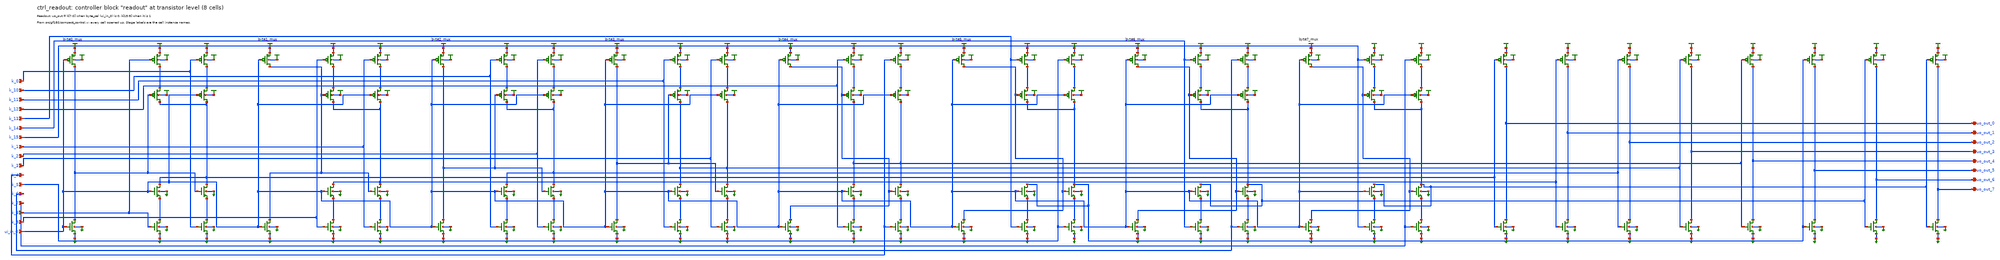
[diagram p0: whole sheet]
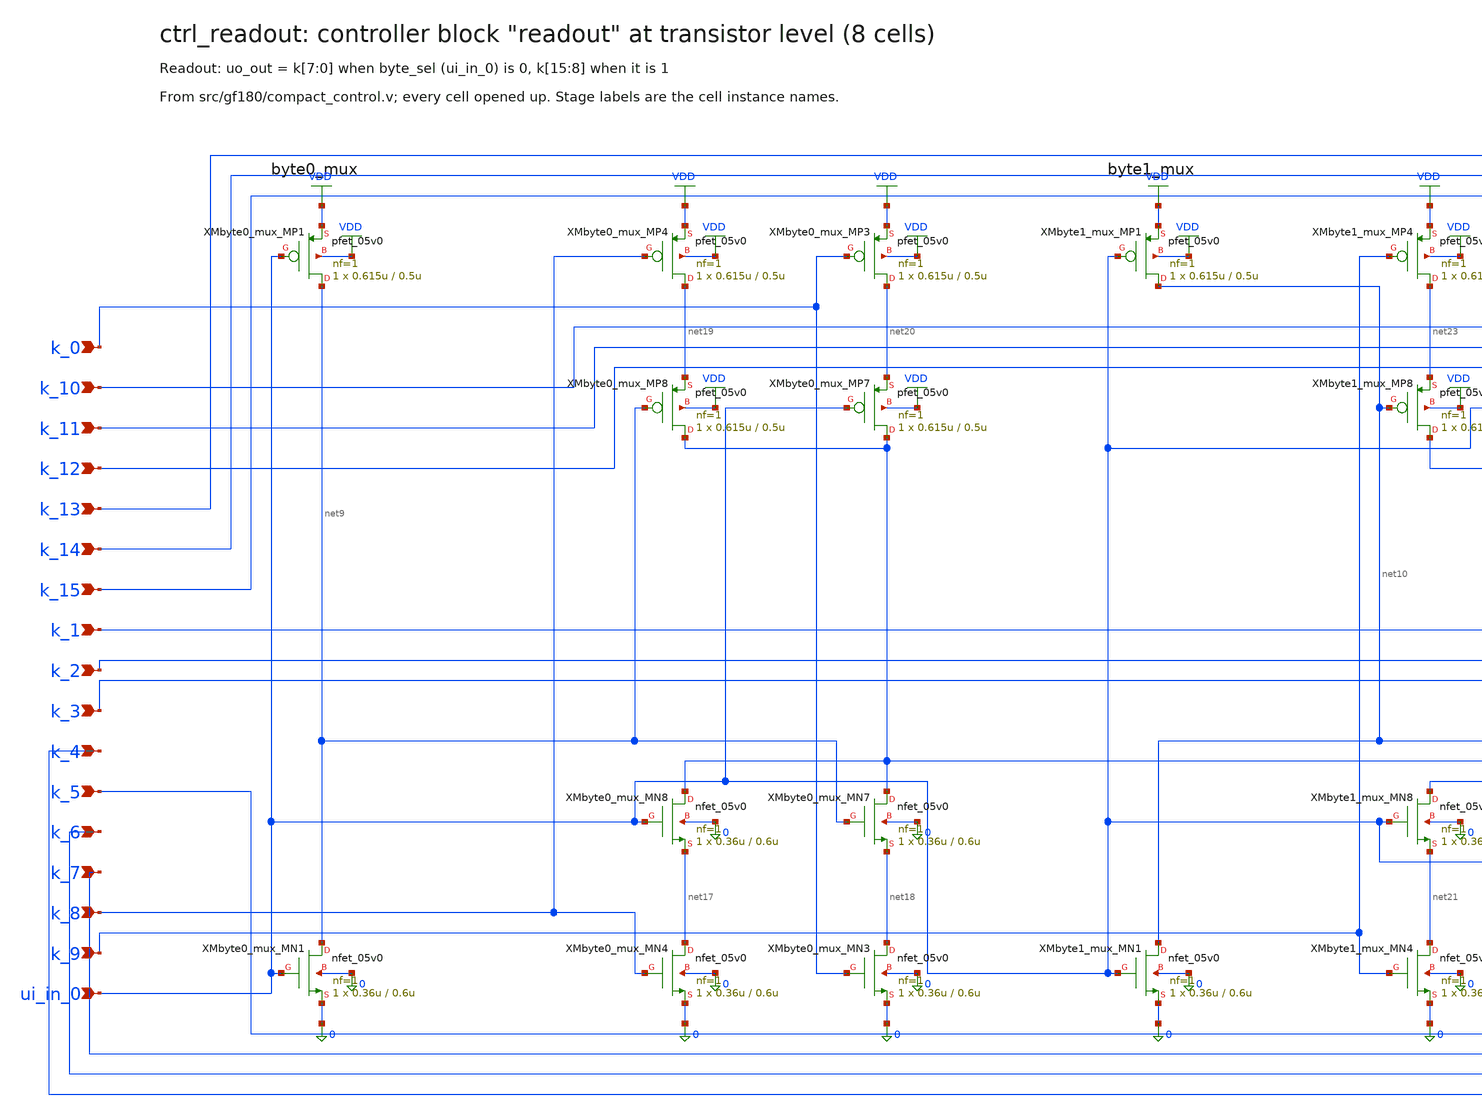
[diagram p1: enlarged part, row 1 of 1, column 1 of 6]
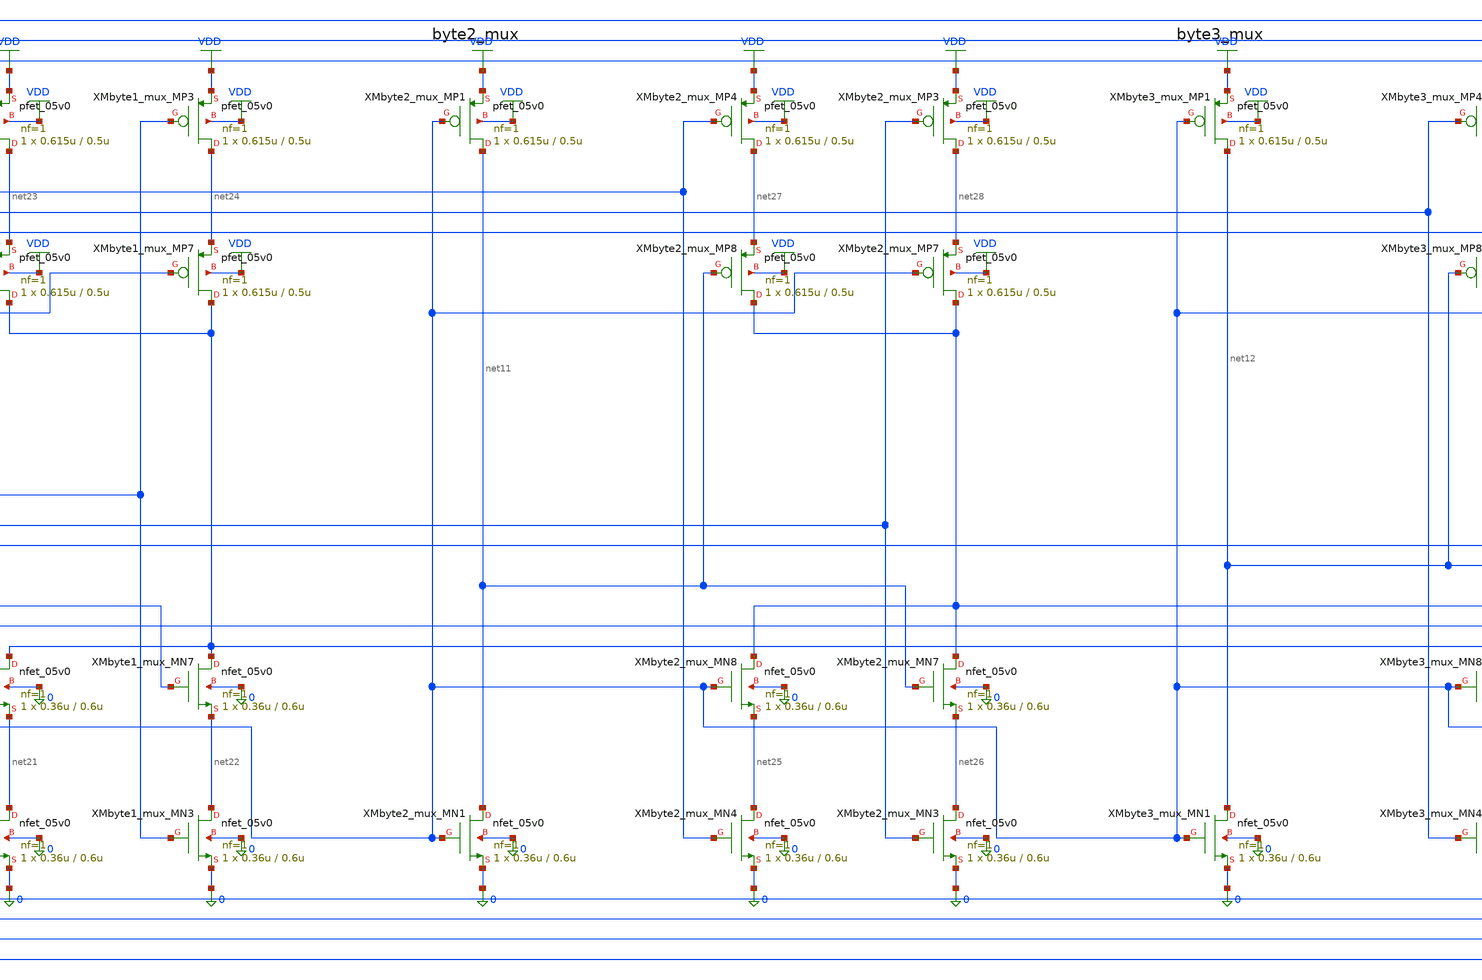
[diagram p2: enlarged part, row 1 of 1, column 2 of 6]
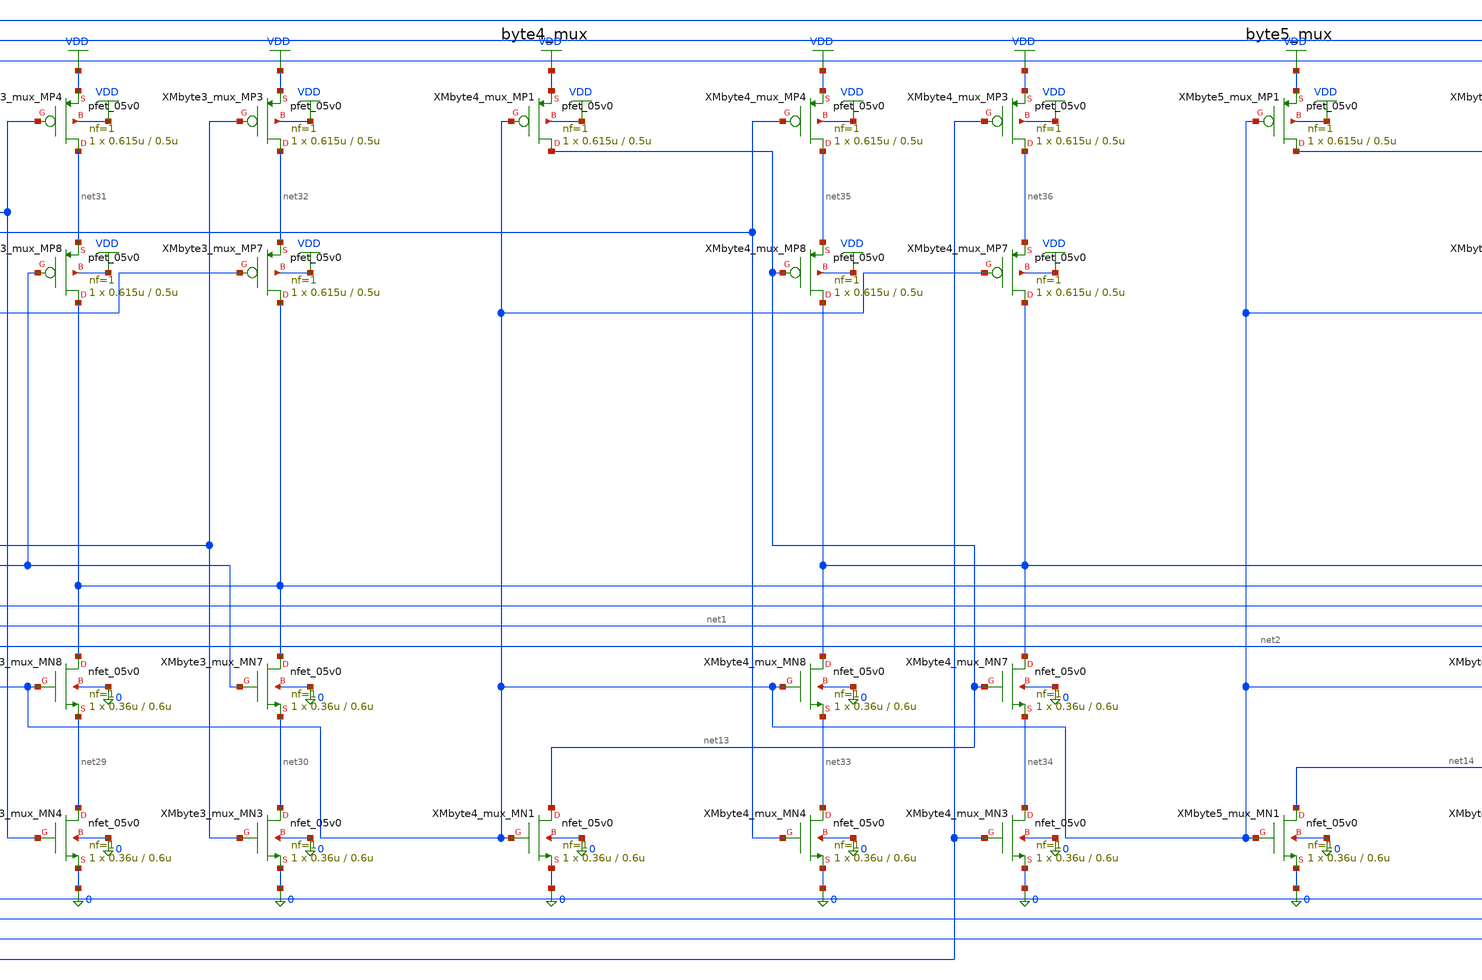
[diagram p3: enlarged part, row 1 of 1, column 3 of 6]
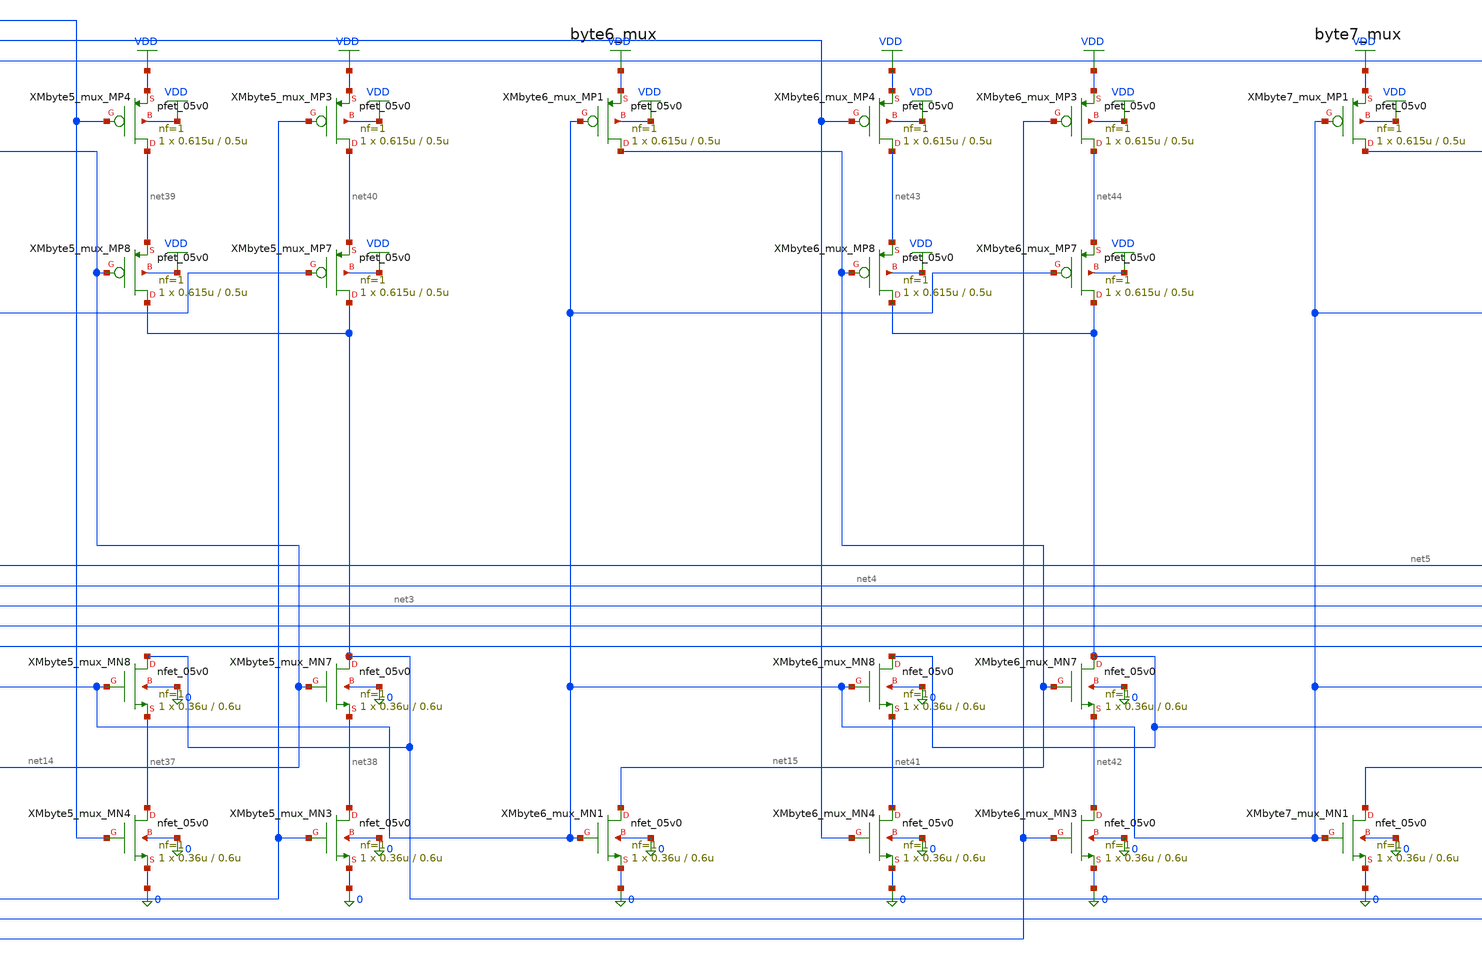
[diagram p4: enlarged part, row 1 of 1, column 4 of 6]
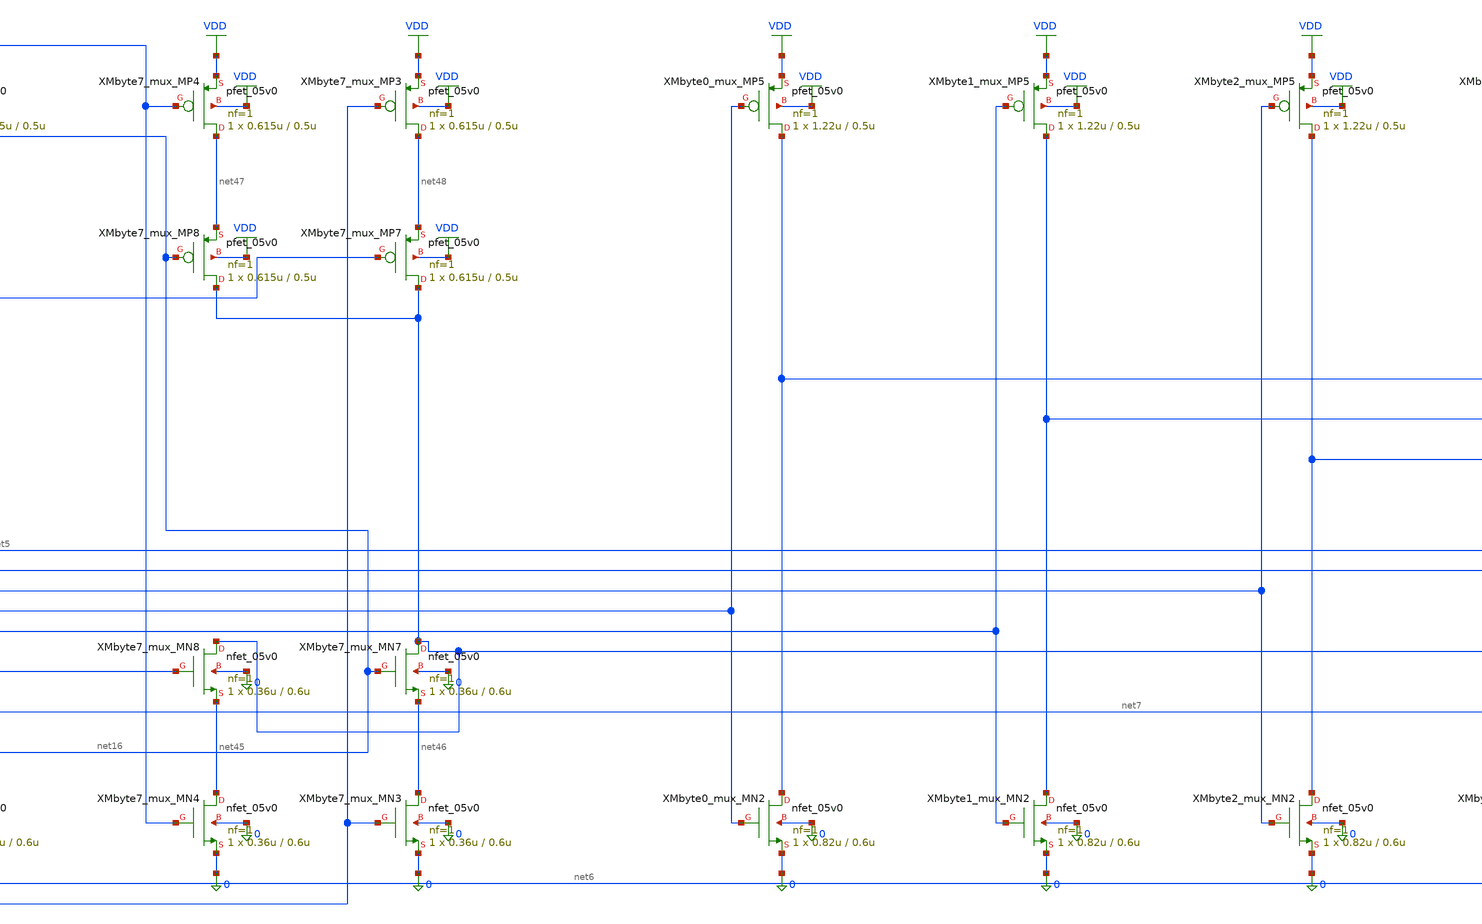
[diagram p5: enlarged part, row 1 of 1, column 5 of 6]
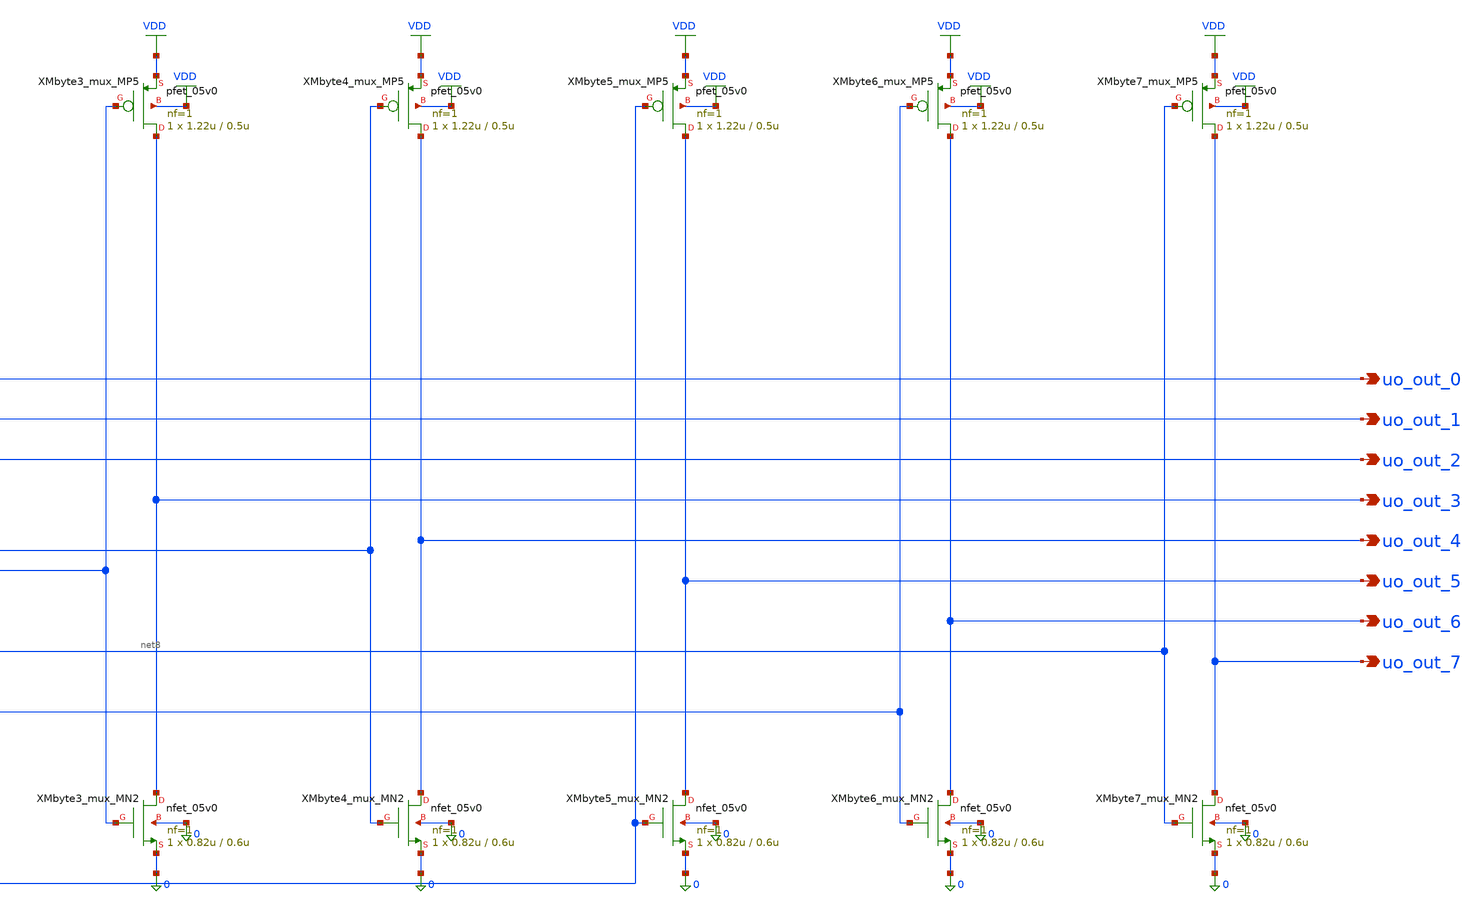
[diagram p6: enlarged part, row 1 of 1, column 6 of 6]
** sch_path: xschem/flat/ctrl_readout.sch
**.subckt ctrl_readout k_0 k_10 k_11 k_12 k_13 k_14 k_15 k_1 k_2 k_3 k_4 k_5 k_6 k_7 k_8 k_9 ui_in_0
*+ uo_out_0 uo_out_1 uo_out_2 uo_out_3 uo_out_4 uo_out_5 uo_out_6 uo_out_7
*.ipin k_0
*.ipin k_10
*.ipin k_11
*.ipin k_12
*.ipin k_13
*.ipin k_14
*.ipin k_15
*.ipin k_1
*.ipin k_2
*.ipin k_3
*.ipin k_4
*.ipin k_5
*.ipin k_6
*.ipin k_7
*.ipin k_8
*.ipin k_9
*.ipin ui_in_0
*.opin uo_out_0
*.opin uo_out_1
*.opin uo_out_2
*.opin uo_out_3
*.opin uo_out_4
*.opin uo_out_5
*.opin uo_out_6
*.opin uo_out_7
XMbyte0_mux_MN2 uo_out_0 net1 0 0 nfet_05v0 L=0.6u W=0.82u nf=1 ad=4.1e-13 as=4.1e-13 pd=2.64e-06
+ ps=2.64e-06 nrd=0 nrs=0 sa=0 sb=0 sd=0 m=1
XMbyte0_mux_MN4 net17 k_8 0 0 nfet_05v0 L=0.6u W=0.36u nf=1 ad=1.8e-13 as=1.8e-13 pd=1.72e-06
+ ps=1.72e-06 nrd=0 nrs=0 sa=0 sb=0 sd=0 m=1
XMbyte0_mux_MN8 net1 ui_in_0 net17 0 nfet_05v0 L=0.6u W=0.36u nf=1 ad=1.8e-13 as=1.8e-13 pd=1.72e-06
+ ps=1.72e-06 nrd=0 nrs=0 sa=0 sb=0 sd=0 m=1
XMbyte0_mux_MN7 net1 net9 net18 0 nfet_05v0 L=0.6u W=0.36u nf=1 ad=1.8e-13 as=1.8e-13 pd=1.72e-06
+ ps=1.72e-06 nrd=0 nrs=0 sa=0 sb=0 sd=0 m=1
XMbyte0_mux_MN3 net18 k_0 0 0 nfet_05v0 L=0.6u W=0.36u nf=1 ad=1.8e-13 as=1.8e-13 pd=1.72e-06
+ ps=1.72e-06 nrd=0 nrs=0 sa=0 sb=0 sd=0 m=1
XMbyte0_mux_MN1 net9 ui_in_0 0 0 nfet_05v0 L=0.6u W=0.36u nf=1 ad=1.8e-13 as=1.8e-13 pd=1.72e-06
+ ps=1.72e-06 nrd=0 nrs=0 sa=0 sb=0 sd=0 m=1
XMbyte0_mux_MP5 uo_out_0 net1 VDD VDD pfet_05v0 L=0.5u W=1.22u nf=1 ad=6.1e-13 as=6.1e-13
+ pd=3.44e-06 ps=3.44e-06 nrd=0 nrs=0 sa=0 sb=0 sd=0 m=1
XMbyte0_mux_MP4 net19 k_8 VDD VDD pfet_05v0 L=0.5u W=0.615u nf=1 ad=3.075e-13 as=3.075e-13
+ pd=2.23e-06 ps=2.23e-06 nrd=0 nrs=0 sa=0 sb=0 sd=0 m=1
XMbyte0_mux_MP8 net1 net9 net19 VDD pfet_05v0 L=0.5u W=0.615u nf=1 ad=3.075e-13 as=3.075e-13
+ pd=2.23e-06 ps=2.23e-06 nrd=0 nrs=0 sa=0 sb=0 sd=0 m=1
XMbyte0_mux_MP7 net1 ui_in_0 net20 VDD pfet_05v0 L=0.5u W=0.615u nf=1 ad=3.075e-13 as=3.075e-13
+ pd=2.23e-06 ps=2.23e-06 nrd=0 nrs=0 sa=0 sb=0 sd=0 m=1
XMbyte0_mux_MP3 net20 k_0 VDD VDD pfet_05v0 L=0.5u W=0.615u nf=1 ad=3.075e-13 as=3.075e-13
+ pd=2.23e-06 ps=2.23e-06 nrd=0 nrs=0 sa=0 sb=0 sd=0 m=1
XMbyte0_mux_MP1 net9 ui_in_0 VDD VDD pfet_05v0 L=0.5u W=0.615u nf=1 ad=3.075e-13 as=3.075e-13
+ pd=2.23e-06 ps=2.23e-06 nrd=0 nrs=0 sa=0 sb=0 sd=0 m=1
XMbyte1_mux_MN2 uo_out_1 net2 0 0 nfet_05v0 L=0.6u W=0.82u nf=1 ad=4.1e-13 as=4.1e-13 pd=2.64e-06
+ ps=2.64e-06 nrd=0 nrs=0 sa=0 sb=0 sd=0 m=1
XMbyte1_mux_MN4 net21 k_9 0 0 nfet_05v0 L=0.6u W=0.36u nf=1 ad=1.8e-13 as=1.8e-13 pd=1.72e-06
+ ps=1.72e-06 nrd=0 nrs=0 sa=0 sb=0 sd=0 m=1
XMbyte1_mux_MN8 net2 ui_in_0 net21 0 nfet_05v0 L=0.6u W=0.36u nf=1 ad=1.8e-13 as=1.8e-13 pd=1.72e-06
+ ps=1.72e-06 nrd=0 nrs=0 sa=0 sb=0 sd=0 m=1
XMbyte1_mux_MN7 net2 net10 net22 0 nfet_05v0 L=0.6u W=0.36u nf=1 ad=1.8e-13 as=1.8e-13 pd=1.72e-06
+ ps=1.72e-06 nrd=0 nrs=0 sa=0 sb=0 sd=0 m=1
XMbyte1_mux_MN3 net22 k_1 0 0 nfet_05v0 L=0.6u W=0.36u nf=1 ad=1.8e-13 as=1.8e-13 pd=1.72e-06
+ ps=1.72e-06 nrd=0 nrs=0 sa=0 sb=0 sd=0 m=1
XMbyte1_mux_MN1 net10 ui_in_0 0 0 nfet_05v0 L=0.6u W=0.36u nf=1 ad=1.8e-13 as=1.8e-13 pd=1.72e-06
+ ps=1.72e-06 nrd=0 nrs=0 sa=0 sb=0 sd=0 m=1
XMbyte1_mux_MP5 uo_out_1 net2 VDD VDD pfet_05v0 L=0.5u W=1.22u nf=1 ad=6.1e-13 as=6.1e-13
+ pd=3.44e-06 ps=3.44e-06 nrd=0 nrs=0 sa=0 sb=0 sd=0 m=1
XMbyte1_mux_MP4 net23 k_9 VDD VDD pfet_05v0 L=0.5u W=0.615u nf=1 ad=3.075e-13 as=3.075e-13
+ pd=2.23e-06 ps=2.23e-06 nrd=0 nrs=0 sa=0 sb=0 sd=0 m=1
XMbyte1_mux_MP8 net2 net10 net23 VDD pfet_05v0 L=0.5u W=0.615u nf=1 ad=3.075e-13 as=3.075e-13
+ pd=2.23e-06 ps=2.23e-06 nrd=0 nrs=0 sa=0 sb=0 sd=0 m=1
XMbyte1_mux_MP7 net2 ui_in_0 net24 VDD pfet_05v0 L=0.5u W=0.615u nf=1 ad=3.075e-13 as=3.075e-13
+ pd=2.23e-06 ps=2.23e-06 nrd=0 nrs=0 sa=0 sb=0 sd=0 m=1
XMbyte1_mux_MP3 net24 k_1 VDD VDD pfet_05v0 L=0.5u W=0.615u nf=1 ad=3.075e-13 as=3.075e-13
+ pd=2.23e-06 ps=2.23e-06 nrd=0 nrs=0 sa=0 sb=0 sd=0 m=1
XMbyte1_mux_MP1 net10 ui_in_0 VDD VDD pfet_05v0 L=0.5u W=0.615u nf=1 ad=3.075e-13 as=3.075e-13
+ pd=2.23e-06 ps=2.23e-06 nrd=0 nrs=0 sa=0 sb=0 sd=0 m=1
XMbyte2_mux_MN2 uo_out_2 net3 0 0 nfet_05v0 L=0.6u W=0.82u nf=1 ad=4.1e-13 as=4.1e-13 pd=2.64e-06
+ ps=2.64e-06 nrd=0 nrs=0 sa=0 sb=0 sd=0 m=1
XMbyte2_mux_MN4 net25 k_10 0 0 nfet_05v0 L=0.6u W=0.36u nf=1 ad=1.8e-13 as=1.8e-13 pd=1.72e-06
+ ps=1.72e-06 nrd=0 nrs=0 sa=0 sb=0 sd=0 m=1
XMbyte2_mux_MN8 net3 ui_in_0 net25 0 nfet_05v0 L=0.6u W=0.36u nf=1 ad=1.8e-13 as=1.8e-13 pd=1.72e-06
+ ps=1.72e-06 nrd=0 nrs=0 sa=0 sb=0 sd=0 m=1
XMbyte2_mux_MN7 net3 net11 net26 0 nfet_05v0 L=0.6u W=0.36u nf=1 ad=1.8e-13 as=1.8e-13 pd=1.72e-06
+ ps=1.72e-06 nrd=0 nrs=0 sa=0 sb=0 sd=0 m=1
XMbyte2_mux_MN3 net26 k_2 0 0 nfet_05v0 L=0.6u W=0.36u nf=1 ad=1.8e-13 as=1.8e-13 pd=1.72e-06
+ ps=1.72e-06 nrd=0 nrs=0 sa=0 sb=0 sd=0 m=1
XMbyte2_mux_MN1 net11 ui_in_0 0 0 nfet_05v0 L=0.6u W=0.36u nf=1 ad=1.8e-13 as=1.8e-13 pd=1.72e-06
+ ps=1.72e-06 nrd=0 nrs=0 sa=0 sb=0 sd=0 m=1
XMbyte2_mux_MP5 uo_out_2 net3 VDD VDD pfet_05v0 L=0.5u W=1.22u nf=1 ad=6.1e-13 as=6.1e-13
+ pd=3.44e-06 ps=3.44e-06 nrd=0 nrs=0 sa=0 sb=0 sd=0 m=1
XMbyte2_mux_MP4 net27 k_10 VDD VDD pfet_05v0 L=0.5u W=0.615u nf=1 ad=3.075e-13 as=3.075e-13
+ pd=2.23e-06 ps=2.23e-06 nrd=0 nrs=0 sa=0 sb=0 sd=0 m=1
XMbyte2_mux_MP8 net3 net11 net27 VDD pfet_05v0 L=0.5u W=0.615u nf=1 ad=3.075e-13 as=3.075e-13
+ pd=2.23e-06 ps=2.23e-06 nrd=0 nrs=0 sa=0 sb=0 sd=0 m=1
XMbyte2_mux_MP7 net3 ui_in_0 net28 VDD pfet_05v0 L=0.5u W=0.615u nf=1 ad=3.075e-13 as=3.075e-13
+ pd=2.23e-06 ps=2.23e-06 nrd=0 nrs=0 sa=0 sb=0 sd=0 m=1
XMbyte2_mux_MP3 net28 k_2 VDD VDD pfet_05v0 L=0.5u W=0.615u nf=1 ad=3.075e-13 as=3.075e-13
+ pd=2.23e-06 ps=2.23e-06 nrd=0 nrs=0 sa=0 sb=0 sd=0 m=1
XMbyte2_mux_MP1 net11 ui_in_0 VDD VDD pfet_05v0 L=0.5u W=0.615u nf=1 ad=3.075e-13 as=3.075e-13
+ pd=2.23e-06 ps=2.23e-06 nrd=0 nrs=0 sa=0 sb=0 sd=0 m=1
XMbyte3_mux_MN2 uo_out_3 net4 0 0 nfet_05v0 L=0.6u W=0.82u nf=1 ad=4.1e-13 as=4.1e-13 pd=2.64e-06
+ ps=2.64e-06 nrd=0 nrs=0 sa=0 sb=0 sd=0 m=1
XMbyte3_mux_MN4 net29 k_11 0 0 nfet_05v0 L=0.6u W=0.36u nf=1 ad=1.8e-13 as=1.8e-13 pd=1.72e-06
+ ps=1.72e-06 nrd=0 nrs=0 sa=0 sb=0 sd=0 m=1
XMbyte3_mux_MN8 net4 ui_in_0 net29 0 nfet_05v0 L=0.6u W=0.36u nf=1 ad=1.8e-13 as=1.8e-13 pd=1.72e-06
+ ps=1.72e-06 nrd=0 nrs=0 sa=0 sb=0 sd=0 m=1
XMbyte3_mux_MN7 net4 net12 net30 0 nfet_05v0 L=0.6u W=0.36u nf=1 ad=1.8e-13 as=1.8e-13 pd=1.72e-06
+ ps=1.72e-06 nrd=0 nrs=0 sa=0 sb=0 sd=0 m=1
XMbyte3_mux_MN3 net30 k_3 0 0 nfet_05v0 L=0.6u W=0.36u nf=1 ad=1.8e-13 as=1.8e-13 pd=1.72e-06
+ ps=1.72e-06 nrd=0 nrs=0 sa=0 sb=0 sd=0 m=1
XMbyte3_mux_MN1 net12 ui_in_0 0 0 nfet_05v0 L=0.6u W=0.36u nf=1 ad=1.8e-13 as=1.8e-13 pd=1.72e-06
+ ps=1.72e-06 nrd=0 nrs=0 sa=0 sb=0 sd=0 m=1
XMbyte3_mux_MP5 uo_out_3 net4 VDD VDD pfet_05v0 L=0.5u W=1.22u nf=1 ad=6.1e-13 as=6.1e-13
+ pd=3.44e-06 ps=3.44e-06 nrd=0 nrs=0 sa=0 sb=0 sd=0 m=1
XMbyte3_mux_MP4 net31 k_11 VDD VDD pfet_05v0 L=0.5u W=0.615u nf=1 ad=3.075e-13 as=3.075e-13
+ pd=2.23e-06 ps=2.23e-06 nrd=0 nrs=0 sa=0 sb=0 sd=0 m=1
XMbyte3_mux_MP8 net4 net12 net31 VDD pfet_05v0 L=0.5u W=0.615u nf=1 ad=3.075e-13 as=3.075e-13
+ pd=2.23e-06 ps=2.23e-06 nrd=0 nrs=0 sa=0 sb=0 sd=0 m=1
XMbyte3_mux_MP7 net4 ui_in_0 net32 VDD pfet_05v0 L=0.5u W=0.615u nf=1 ad=3.075e-13 as=3.075e-13
+ pd=2.23e-06 ps=2.23e-06 nrd=0 nrs=0 sa=0 sb=0 sd=0 m=1
XMbyte3_mux_MP3 net32 k_3 VDD VDD pfet_05v0 L=0.5u W=0.615u nf=1 ad=3.075e-13 as=3.075e-13
+ pd=2.23e-06 ps=2.23e-06 nrd=0 nrs=0 sa=0 sb=0 sd=0 m=1
XMbyte3_mux_MP1 net12 ui_in_0 VDD VDD pfet_05v0 L=0.5u W=0.615u nf=1 ad=3.075e-13 as=3.075e-13
+ pd=2.23e-06 ps=2.23e-06 nrd=0 nrs=0 sa=0 sb=0 sd=0 m=1
XMbyte4_mux_MN2 uo_out_4 net5 0 0 nfet_05v0 L=0.6u W=0.82u nf=1 ad=4.1e-13 as=4.1e-13 pd=2.64e-06
+ ps=2.64e-06 nrd=0 nrs=0 sa=0 sb=0 sd=0 m=1
XMbyte4_mux_MN4 net33 k_12 0 0 nfet_05v0 L=0.6u W=0.36u nf=1 ad=1.8e-13 as=1.8e-13 pd=1.72e-06
+ ps=1.72e-06 nrd=0 nrs=0 sa=0 sb=0 sd=0 m=1
XMbyte4_mux_MN8 net5 ui_in_0 net33 0 nfet_05v0 L=0.6u W=0.36u nf=1 ad=1.8e-13 as=1.8e-13 pd=1.72e-06
+ ps=1.72e-06 nrd=0 nrs=0 sa=0 sb=0 sd=0 m=1
XMbyte4_mux_MN7 net5 net13 net34 0 nfet_05v0 L=0.6u W=0.36u nf=1 ad=1.8e-13 as=1.8e-13 pd=1.72e-06
+ ps=1.72e-06 nrd=0 nrs=0 sa=0 sb=0 sd=0 m=1
XMbyte4_mux_MN3 net34 k_4 0 0 nfet_05v0 L=0.6u W=0.36u nf=1 ad=1.8e-13 as=1.8e-13 pd=1.72e-06
+ ps=1.72e-06 nrd=0 nrs=0 sa=0 sb=0 sd=0 m=1
XMbyte4_mux_MN1 net13 ui_in_0 0 0 nfet_05v0 L=0.6u W=0.36u nf=1 ad=1.8e-13 as=1.8e-13 pd=1.72e-06
+ ps=1.72e-06 nrd=0 nrs=0 sa=0 sb=0 sd=0 m=1
XMbyte4_mux_MP5 uo_out_4 net5 VDD VDD pfet_05v0 L=0.5u W=1.22u nf=1 ad=6.1e-13 as=6.1e-13
+ pd=3.44e-06 ps=3.44e-06 nrd=0 nrs=0 sa=0 sb=0 sd=0 m=1
XMbyte4_mux_MP4 net35 k_12 VDD VDD pfet_05v0 L=0.5u W=0.615u nf=1 ad=3.075e-13 as=3.075e-13
+ pd=2.23e-06 ps=2.23e-06 nrd=0 nrs=0 sa=0 sb=0 sd=0 m=1
XMbyte4_mux_MP8 net5 net13 net35 VDD pfet_05v0 L=0.5u W=0.615u nf=1 ad=3.075e-13 as=3.075e-13
+ pd=2.23e-06 ps=2.23e-06 nrd=0 nrs=0 sa=0 sb=0 sd=0 m=1
XMbyte4_mux_MP7 net5 ui_in_0 net36 VDD pfet_05v0 L=0.5u W=0.615u nf=1 ad=3.075e-13 as=3.075e-13
+ pd=2.23e-06 ps=2.23e-06 nrd=0 nrs=0 sa=0 sb=0 sd=0 m=1
XMbyte4_mux_MP3 net36 k_4 VDD VDD pfet_05v0 L=0.5u W=0.615u nf=1 ad=3.075e-13 as=3.075e-13
+ pd=2.23e-06 ps=2.23e-06 nrd=0 nrs=0 sa=0 sb=0 sd=0 m=1
XMbyte4_mux_MP1 net13 ui_in_0 VDD VDD pfet_05v0 L=0.5u W=0.615u nf=1 ad=3.075e-13 as=3.075e-13
+ pd=2.23e-06 ps=2.23e-06 nrd=0 nrs=0 sa=0 sb=0 sd=0 m=1
XMbyte5_mux_MN2 uo_out_5 net6 0 0 nfet_05v0 L=0.6u W=0.82u nf=1 ad=4.1e-13 as=4.1e-13 pd=2.64e-06
+ ps=2.64e-06 nrd=0 nrs=0 sa=0 sb=0 sd=0 m=1
XMbyte5_mux_MN4 net37 k_13 0 0 nfet_05v0 L=0.6u W=0.36u nf=1 ad=1.8e-13 as=1.8e-13 pd=1.72e-06
+ ps=1.72e-06 nrd=0 nrs=0 sa=0 sb=0 sd=0 m=1
XMbyte5_mux_MN8 net6 ui_in_0 net37 0 nfet_05v0 L=0.6u W=0.36u nf=1 ad=1.8e-13 as=1.8e-13 pd=1.72e-06
+ ps=1.72e-06 nrd=0 nrs=0 sa=0 sb=0 sd=0 m=1
XMbyte5_mux_MN7 net6 net14 net38 0 nfet_05v0 L=0.6u W=0.36u nf=1 ad=1.8e-13 as=1.8e-13 pd=1.72e-06
+ ps=1.72e-06 nrd=0 nrs=0 sa=0 sb=0 sd=0 m=1
XMbyte5_mux_MN3 net38 k_5 0 0 nfet_05v0 L=0.6u W=0.36u nf=1 ad=1.8e-13 as=1.8e-13 pd=1.72e-06
+ ps=1.72e-06 nrd=0 nrs=0 sa=0 sb=0 sd=0 m=1
XMbyte5_mux_MN1 net14 ui_in_0 0 0 nfet_05v0 L=0.6u W=0.36u nf=1 ad=1.8e-13 as=1.8e-13 pd=1.72e-06
+ ps=1.72e-06 nrd=0 nrs=0 sa=0 sb=0 sd=0 m=1
XMbyte5_mux_MP5 uo_out_5 net6 VDD VDD pfet_05v0 L=0.5u W=1.22u nf=1 ad=6.1e-13 as=6.1e-13
+ pd=3.44e-06 ps=3.44e-06 nrd=0 nrs=0 sa=0 sb=0 sd=0 m=1
XMbyte5_mux_MP4 net39 k_13 VDD VDD pfet_05v0 L=0.5u W=0.615u nf=1 ad=3.075e-13 as=3.075e-13
+ pd=2.23e-06 ps=2.23e-06 nrd=0 nrs=0 sa=0 sb=0 sd=0 m=1
XMbyte5_mux_MP8 net6 net14 net39 VDD pfet_05v0 L=0.5u W=0.615u nf=1 ad=3.075e-13 as=3.075e-13
+ pd=2.23e-06 ps=2.23e-06 nrd=0 nrs=0 sa=0 sb=0 sd=0 m=1
XMbyte5_mux_MP7 net6 ui_in_0 net40 VDD pfet_05v0 L=0.5u W=0.615u nf=1 ad=3.075e-13 as=3.075e-13
+ pd=2.23e-06 ps=2.23e-06 nrd=0 nrs=0 sa=0 sb=0 sd=0 m=1
XMbyte5_mux_MP3 net40 k_5 VDD VDD pfet_05v0 L=0.5u W=0.615u nf=1 ad=3.075e-13 as=3.075e-13
+ pd=2.23e-06 ps=2.23e-06 nrd=0 nrs=0 sa=0 sb=0 sd=0 m=1
XMbyte5_mux_MP1 net14 ui_in_0 VDD VDD pfet_05v0 L=0.5u W=0.615u nf=1 ad=3.075e-13 as=3.075e-13
+ pd=2.23e-06 ps=2.23e-06 nrd=0 nrs=0 sa=0 sb=0 sd=0 m=1
XMbyte6_mux_MN2 uo_out_6 net7 0 0 nfet_05v0 L=0.6u W=0.82u nf=1 ad=4.1e-13 as=4.1e-13 pd=2.64e-06
+ ps=2.64e-06 nrd=0 nrs=0 sa=0 sb=0 sd=0 m=1
XMbyte6_mux_MN4 net41 k_14 0 0 nfet_05v0 L=0.6u W=0.36u nf=1 ad=1.8e-13 as=1.8e-13 pd=1.72e-06
+ ps=1.72e-06 nrd=0 nrs=0 sa=0 sb=0 sd=0 m=1
XMbyte6_mux_MN8 net7 ui_in_0 net41 0 nfet_05v0 L=0.6u W=0.36u nf=1 ad=1.8e-13 as=1.8e-13 pd=1.72e-06
+ ps=1.72e-06 nrd=0 nrs=0 sa=0 sb=0 sd=0 m=1
XMbyte6_mux_MN7 net7 net15 net42 0 nfet_05v0 L=0.6u W=0.36u nf=1 ad=1.8e-13 as=1.8e-13 pd=1.72e-06
+ ps=1.72e-06 nrd=0 nrs=0 sa=0 sb=0 sd=0 m=1
XMbyte6_mux_MN3 net42 k_6 0 0 nfet_05v0 L=0.6u W=0.36u nf=1 ad=1.8e-13 as=1.8e-13 pd=1.72e-06
+ ps=1.72e-06 nrd=0 nrs=0 sa=0 sb=0 sd=0 m=1
XMbyte6_mux_MN1 net15 ui_in_0 0 0 nfet_05v0 L=0.6u W=0.36u nf=1 ad=1.8e-13 as=1.8e-13 pd=1.72e-06
+ ps=1.72e-06 nrd=0 nrs=0 sa=0 sb=0 sd=0 m=1
XMbyte6_mux_MP5 uo_out_6 net7 VDD VDD pfet_05v0 L=0.5u W=1.22u nf=1 ad=6.1e-13 as=6.1e-13
+ pd=3.44e-06 ps=3.44e-06 nrd=0 nrs=0 sa=0 sb=0 sd=0 m=1
XMbyte6_mux_MP4 net43 k_14 VDD VDD pfet_05v0 L=0.5u W=0.615u nf=1 ad=3.075e-13 as=3.075e-13
+ pd=2.23e-06 ps=2.23e-06 nrd=0 nrs=0 sa=0 sb=0 sd=0 m=1
XMbyte6_mux_MP8 net7 net15 net43 VDD pfet_05v0 L=0.5u W=0.615u nf=1 ad=3.075e-13 as=3.075e-13
+ pd=2.23e-06 ps=2.23e-06 nrd=0 nrs=0 sa=0 sb=0 sd=0 m=1
XMbyte6_mux_MP7 net7 ui_in_0 net44 VDD pfet_05v0 L=0.5u W=0.615u nf=1 ad=3.075e-13 as=3.075e-13
+ pd=2.23e-06 ps=2.23e-06 nrd=0 nrs=0 sa=0 sb=0 sd=0 m=1
XMbyte6_mux_MP3 net44 k_6 VDD VDD pfet_05v0 L=0.5u W=0.615u nf=1 ad=3.075e-13 as=3.075e-13
+ pd=2.23e-06 ps=2.23e-06 nrd=0 nrs=0 sa=0 sb=0 sd=0 m=1
XMbyte6_mux_MP1 net15 ui_in_0 VDD VDD pfet_05v0 L=0.5u W=0.615u nf=1 ad=3.075e-13 as=3.075e-13
+ pd=2.23e-06 ps=2.23e-06 nrd=0 nrs=0 sa=0 sb=0 sd=0 m=1
XMbyte7_mux_MN2 uo_out_7 net8 0 0 nfet_05v0 L=0.6u W=0.82u nf=1 ad=4.1e-13 as=4.1e-13 pd=2.64e-06
+ ps=2.64e-06 nrd=0 nrs=0 sa=0 sb=0 sd=0 m=1
XMbyte7_mux_MN4 net45 k_15 0 0 nfet_05v0 L=0.6u W=0.36u nf=1 ad=1.8e-13 as=1.8e-13 pd=1.72e-06
+ ps=1.72e-06 nrd=0 nrs=0 sa=0 sb=0 sd=0 m=1
XMbyte7_mux_MN8 net8 ui_in_0 net45 0 nfet_05v0 L=0.6u W=0.36u nf=1 ad=1.8e-13 as=1.8e-13 pd=1.72e-06
+ ps=1.72e-06 nrd=0 nrs=0 sa=0 sb=0 sd=0 m=1
XMbyte7_mux_MN7 net8 net16 net46 0 nfet_05v0 L=0.6u W=0.36u nf=1 ad=1.8e-13 as=1.8e-13 pd=1.72e-06
+ ps=1.72e-06 nrd=0 nrs=0 sa=0 sb=0 sd=0 m=1
XMbyte7_mux_MN3 net46 k_7 0 0 nfet_05v0 L=0.6u W=0.36u nf=1 ad=1.8e-13 as=1.8e-13 pd=1.72e-06
+ ps=1.72e-06 nrd=0 nrs=0 sa=0 sb=0 sd=0 m=1
XMbyte7_mux_MN1 net16 ui_in_0 0 0 nfet_05v0 L=0.6u W=0.36u nf=1 ad=1.8e-13 as=1.8e-13 pd=1.72e-06
+ ps=1.72e-06 nrd=0 nrs=0 sa=0 sb=0 sd=0 m=1
XMbyte7_mux_MP5 uo_out_7 net8 VDD VDD pfet_05v0 L=0.5u W=1.22u nf=1 ad=6.1e-13 as=6.1e-13
+ pd=3.44e-06 ps=3.44e-06 nrd=0 nrs=0 sa=0 sb=0 sd=0 m=1
XMbyte7_mux_MP4 net47 k_15 VDD VDD pfet_05v0 L=0.5u W=0.615u nf=1 ad=3.075e-13 as=3.075e-13
+ pd=2.23e-06 ps=2.23e-06 nrd=0 nrs=0 sa=0 sb=0 sd=0 m=1
XMbyte7_mux_MP8 net8 net16 net47 VDD pfet_05v0 L=0.5u W=0.615u nf=1 ad=3.075e-13 as=3.075e-13
+ pd=2.23e-06 ps=2.23e-06 nrd=0 nrs=0 sa=0 sb=0 sd=0 m=1
XMbyte7_mux_MP7 net8 ui_in_0 net48 VDD pfet_05v0 L=0.5u W=0.615u nf=1 ad=3.075e-13 as=3.075e-13
+ pd=2.23e-06 ps=2.23e-06 nrd=0 nrs=0 sa=0 sb=0 sd=0 m=1
XMbyte7_mux_MP3 net48 k_7 VDD VDD pfet_05v0 L=0.5u W=0.615u nf=1 ad=3.075e-13 as=3.075e-13
+ pd=2.23e-06 ps=2.23e-06 nrd=0 nrs=0 sa=0 sb=0 sd=0 m=1
XMbyte7_mux_MP1 net16 ui_in_0 VDD VDD pfet_05v0 L=0.5u W=0.615u nf=1 ad=3.075e-13 as=3.075e-13
+ pd=2.23e-06 ps=2.23e-06 nrd=0 nrs=0 sa=0 sb=0 sd=0 m=1
**.ends
.GLOBAL VDD
.end
